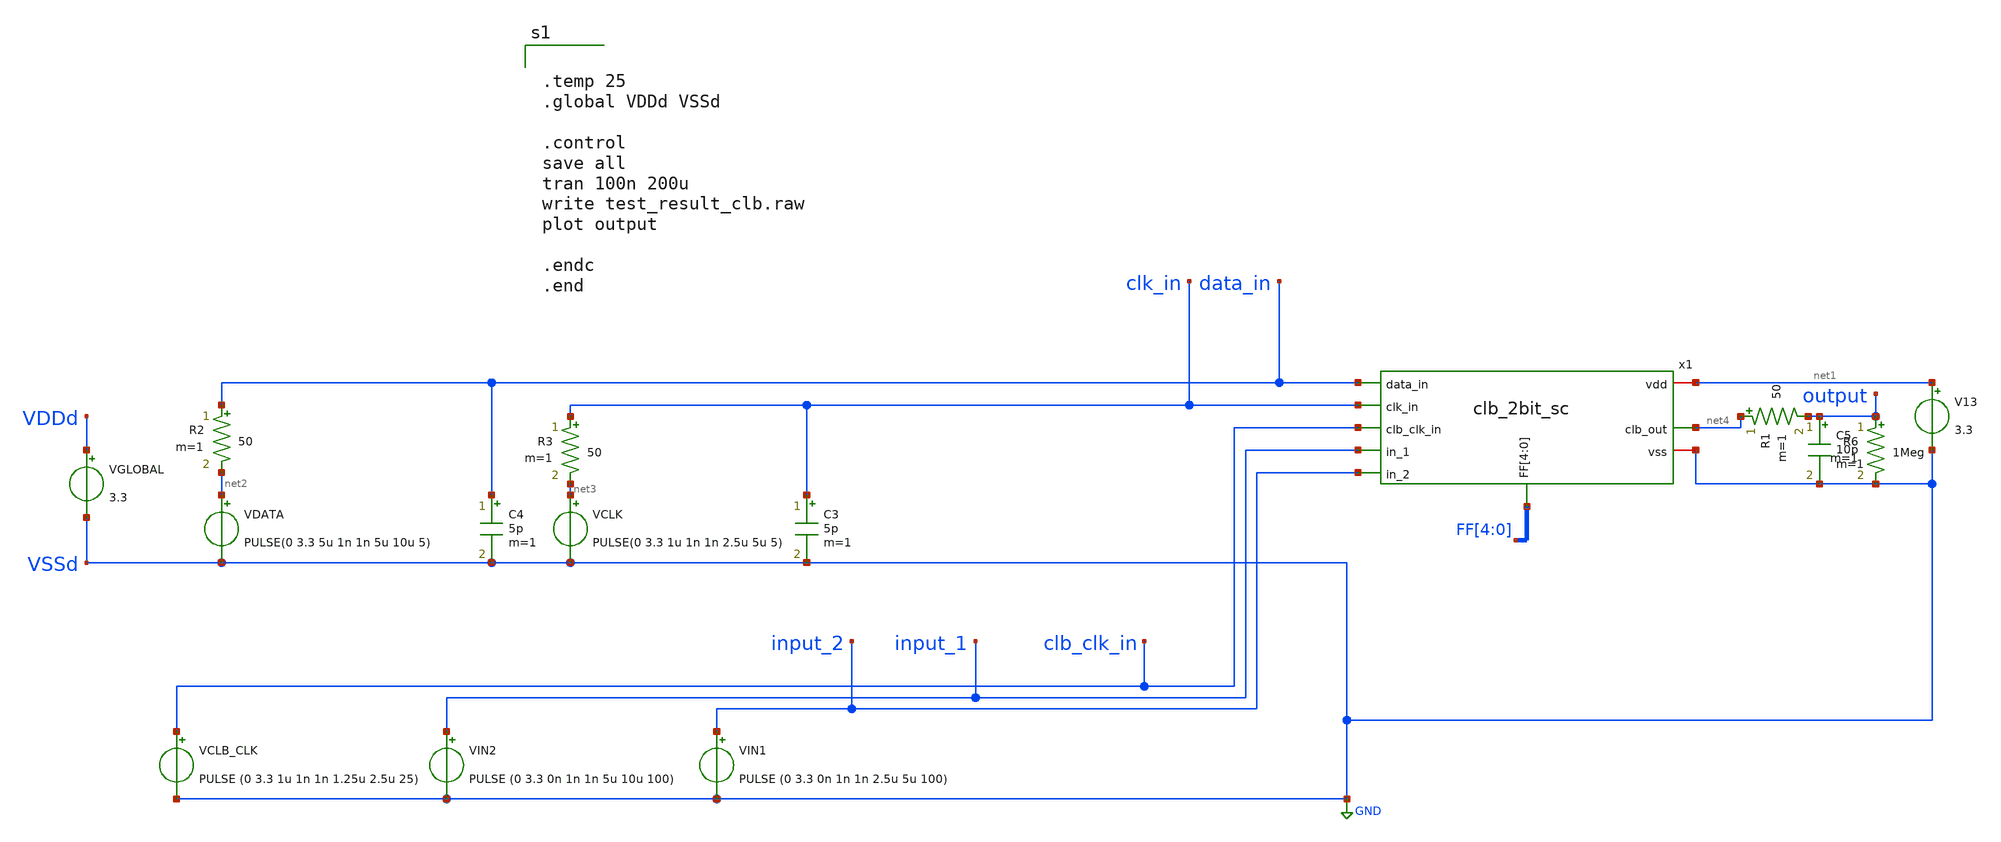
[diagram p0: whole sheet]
** sch_path: designs/libs/tb_fpga/tb_clb/clb_2bit_sc_tb.sch
**.subckt clb_2bit_sc_tb
C3 clk_in GND 5p m=1
C4 data_in GND 5p m=1
VCLK net3 GND PULSE(0 3.3 1u 1n 1n 2.5u 5u 5)
VDATA net2 GND PULSE(0 3.3 5u 1n 1n 5u 10u 5)
V13 net1 GND 3.3
C5 output GND 10p m=1
R1 net4 output 50 m=1
R2 data_in net2 50 m=1
R3 clk_in net3 50 m=1
R6 output GND 1Meg m=1
VIN1 input_2 GND PULSE (0 3.3 0n 1n 1n 2.5u 5u 100)
VIN2 input_1 GND PULSE (0 3.3 0n 1n 1n 5u 10u 100)
VCLB_CLK clb_clk_in GND PULSE (0 3.3 1u 1n 1n 1.25u 2.5u 25)
x1 net1 FF[4] FF[3] FF[2] FF[1] FF[0] clb_clk_in clk_in data_in net4 input_1 input_2 GND clb_2bit_sc
VGLOBAL VDDd GND 3.3
**** begin user architecture code


.temp 25
.global VDDd VSSd

.control
save all
tran 100n 200u
write test_result_clb.raw
plot output

.endc
.end



.include $::180MCU_MODELS/design.ngspice
.include /foss/pdks/gf180mcuD/libs.ref/gf180mcu_fd_sc_mcu9t5v0/spice/gf180mcu_fd_sc_mcu9t5v0.spice
.lib $::180MCU_MODELS/sm141064.ngspice typical
.lib $::180MCU_MODELS/sm141064.ngspice cap_mim
.lib $::180MCU_MODELS/sm141064.ngspice res_typical
.lib $::180MCU_MODELS/sm141064.ngspice moscap_typical
.lib $::180MCU_MODELS/sm141064.ngspice mimcap_typical
* .lib $::180MCU_MODELS/sm141064.ngspice res_statistical

**** end user architecture code
**.ends
.GLOBAL GND
.end
